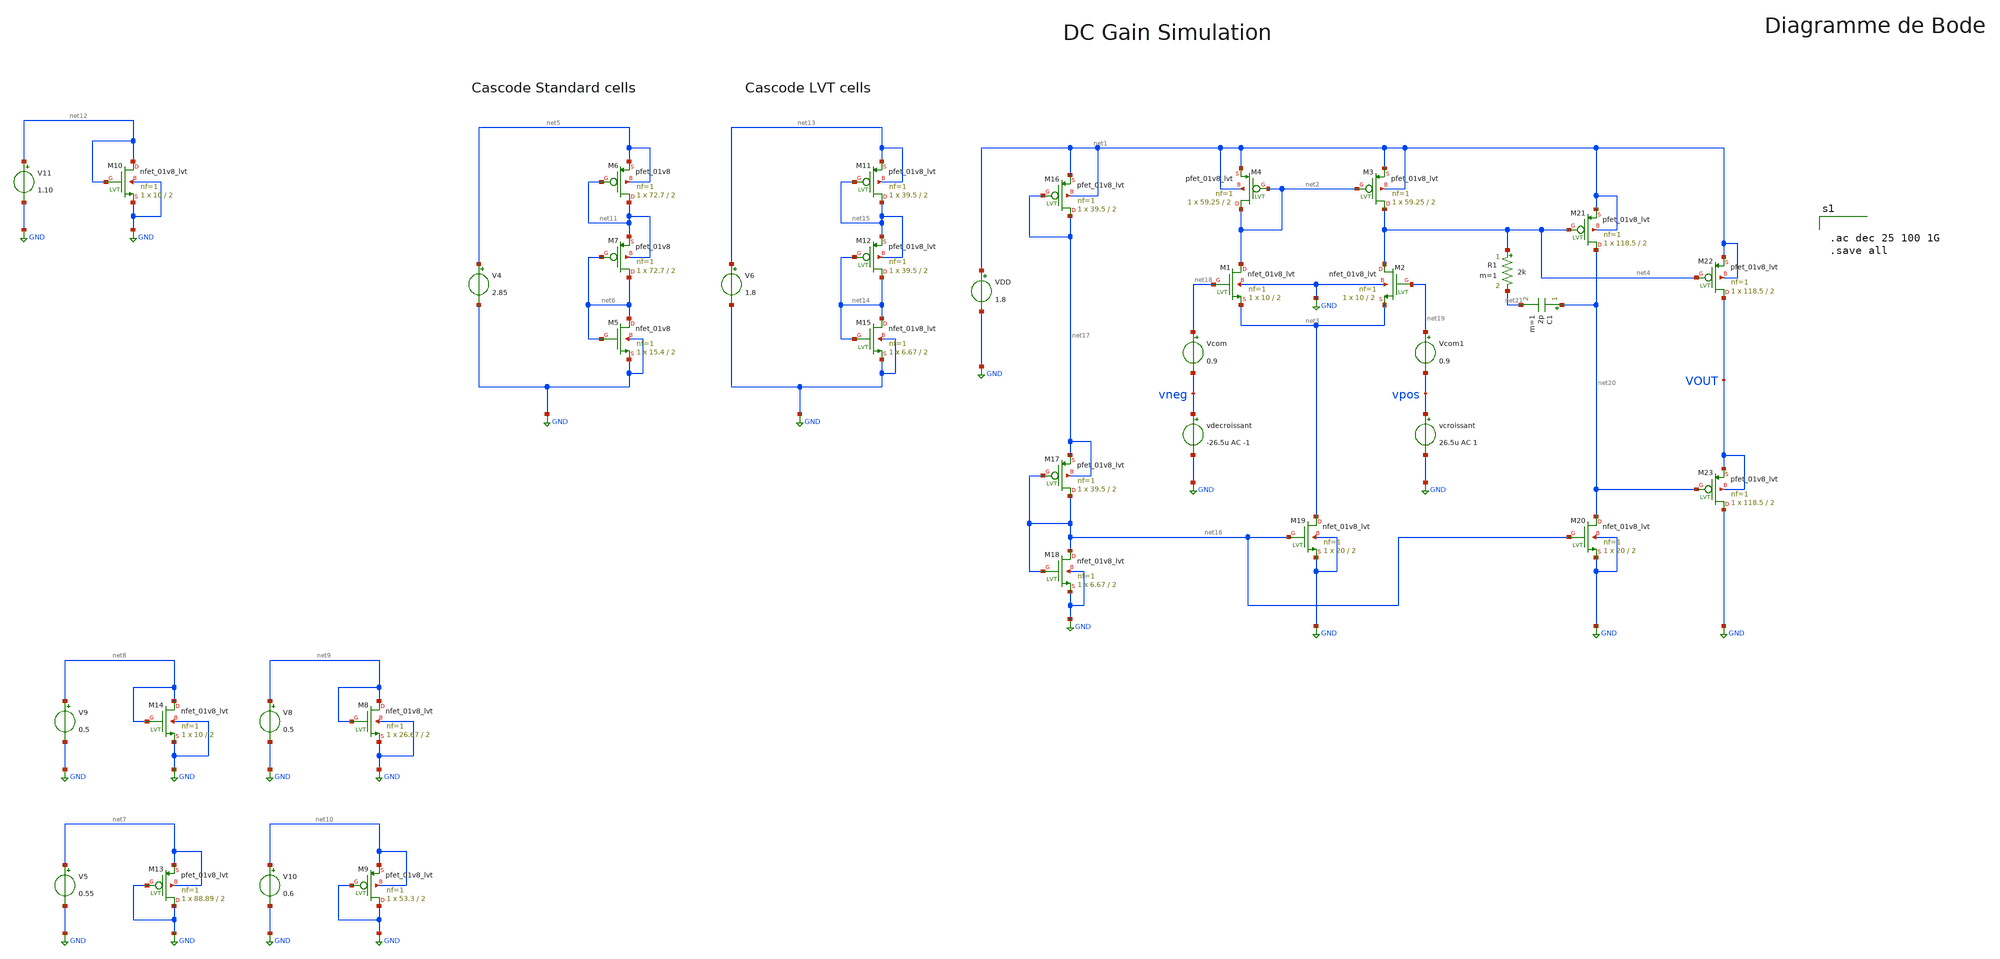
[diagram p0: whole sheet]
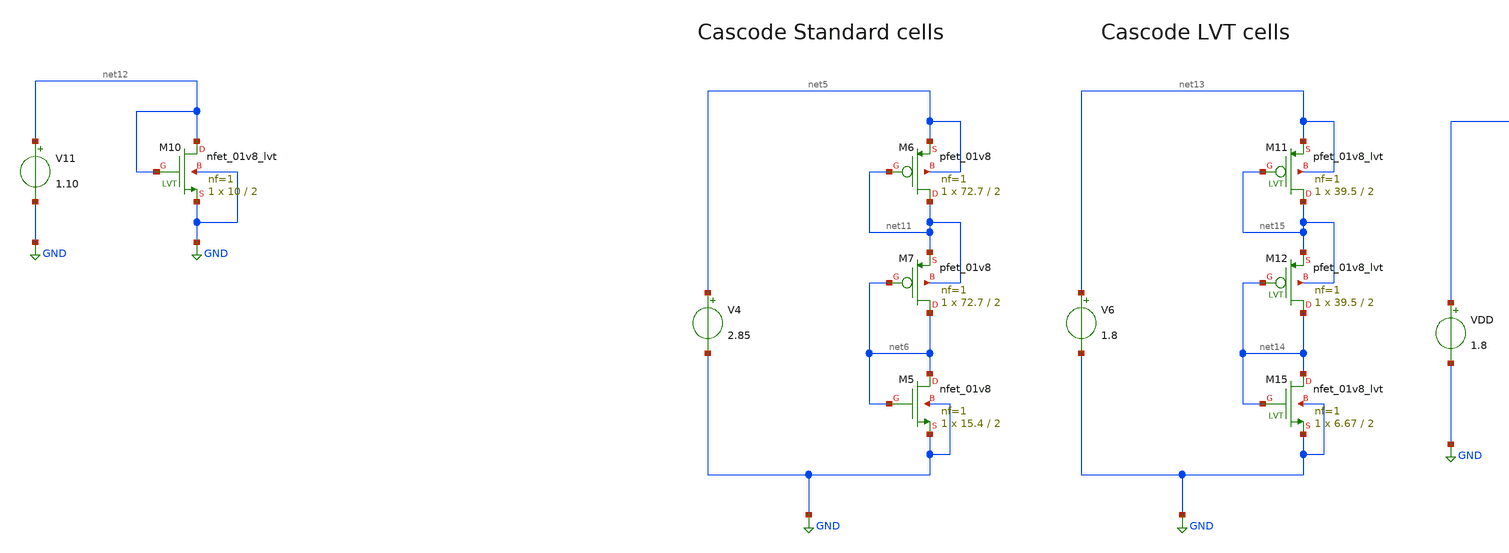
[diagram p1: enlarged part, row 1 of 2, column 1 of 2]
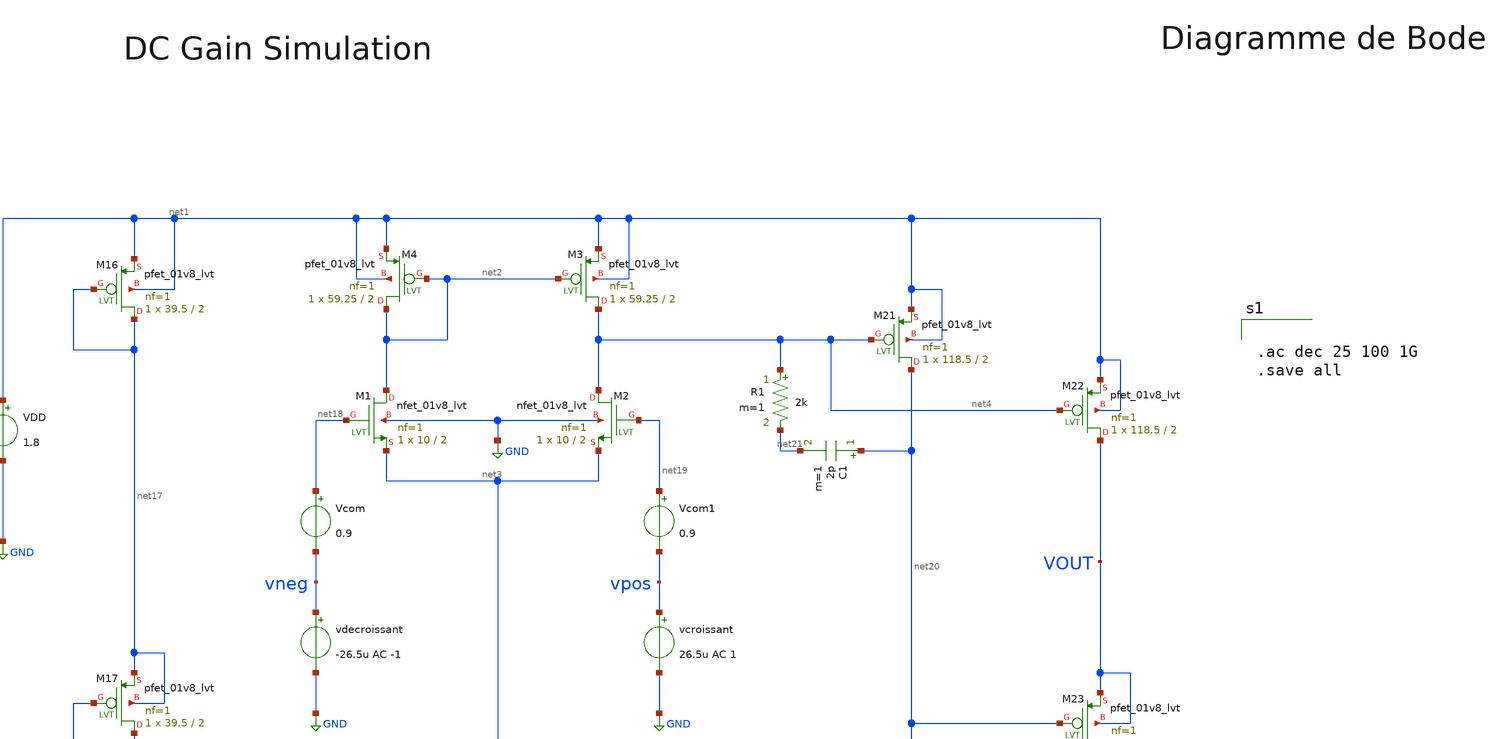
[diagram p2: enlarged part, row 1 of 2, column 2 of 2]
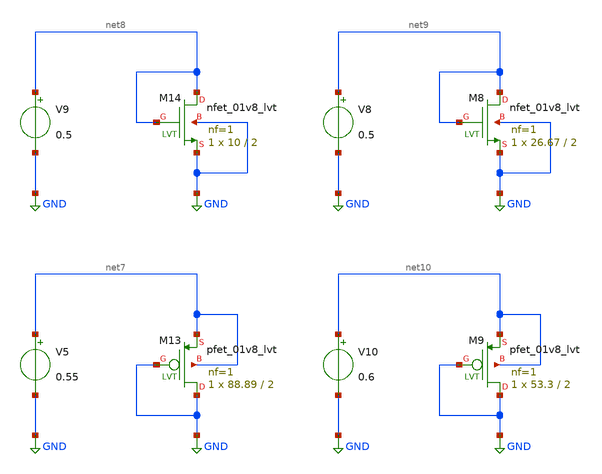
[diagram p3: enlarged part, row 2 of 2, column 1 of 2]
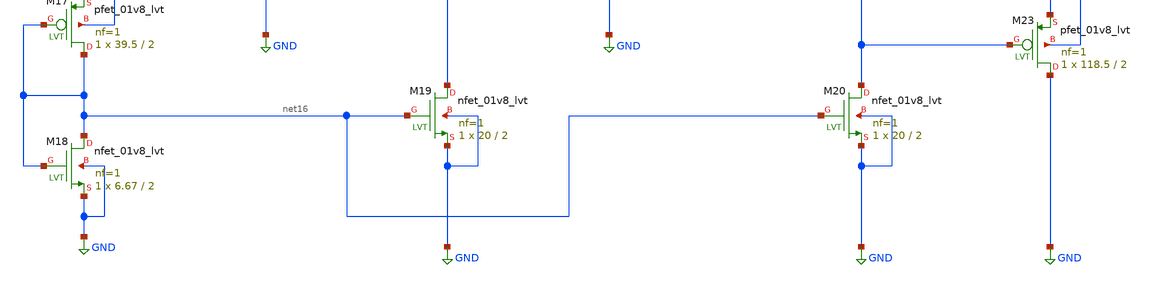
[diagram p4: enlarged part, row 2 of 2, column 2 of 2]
** sch_path: Paire_diff.sch
**.subckt Paire_diff
VDD net1 GND 1.8
V4 net5 GND 2.85
XM5 net6 net6 GND GND sky130_fd_pr__nfet_01v8 L=2 W=15.4 nf=1 ad='int((nf+1)/2) * W/nf * 0.29' as='int((nf+2)/2) * W/nf * 0.29'
+ pd='2*int((nf+1)/2) * (W/nf + 0.29)' ps='2*int((nf+2)/2) * (W/nf + 0.29)' nrd='0.29 / W' nrs='0.29 / W'
+ sa=0 sb=0 sd=0 mult=1 m=1
XM7 net6 net6 net11 net11 sky130_fd_pr__pfet_01v8 L=2 W=72.7 nf=1 ad='int((nf+1)/2) * W/nf * 0.29' as='int((nf+2)/2) * W/nf * 0.29'
+ pd='2*int((nf+1)/2) * (W/nf + 0.29)' ps='2*int((nf+2)/2) * (W/nf + 0.29)' nrd='0.29 / W' nrs='0.29 / W'
+ sa=0 sb=0 sd=0 mult=1 m=1
V5 net7 GND 0.55
V9 net8 GND 0.5
V8 net9 GND 0.5
V10 net10 GND 0.6
XM6 net11 net11 net5 net5 sky130_fd_pr__pfet_01v8 L=2 W=72.7 nf=1 ad='int((nf+1)/2) * W/nf * 0.29' as='int((nf+2)/2) * W/nf * 0.29'
+ pd='2*int((nf+1)/2) * (W/nf + 0.29)' ps='2*int((nf+2)/2) * (W/nf + 0.29)' nrd='0.29 / W' nrs='0.29 / W'
+ sa=0 sb=0 sd=0 mult=1 m=1
XM13 GND GND net7 net7 sky130_fd_pr__pfet_01v8_lvt L=2 W=88.89 nf=1 ad='int((nf+1)/2) * W/nf * 0.29'
+ as='int((nf+2)/2) * W/nf * 0.29' pd='2*int((nf+1)/2) * (W/nf + 0.29)' ps='2*int((nf+2)/2) * (W/nf + 0.29)'
+ nrd='0.29 / W' nrs='0.29 / W' sa=0 sb=0 sd=0 mult=1 m=1
XM14 net8 net8 GND GND sky130_fd_pr__nfet_01v8_lvt L=2 W=10 nf=1 ad='int((nf+1)/2) * W/nf * 0.29' as='int((nf+2)/2) * W/nf * 0.29'
+ pd='2*int((nf+1)/2) * (W/nf + 0.29)' ps='2*int((nf+2)/2) * (W/nf + 0.29)' nrd='0.29 / W' nrs='0.29 / W'
+ sa=0 sb=0 sd=0 mult=1 m=1
XM8 net9 net9 GND GND sky130_fd_pr__nfet_01v8_lvt L=2 W=26.67 nf=1 ad='int((nf+1)/2) * W/nf * 0.29' as='int((nf+2)/2) * W/nf * 0.29'
+ pd='2*int((nf+1)/2) * (W/nf + 0.29)' ps='2*int((nf+2)/2) * (W/nf + 0.29)' nrd='0.29 / W' nrs='0.29 / W'
+ sa=0 sb=0 sd=0 mult=1 m=1
XM9 GND GND net10 net10 sky130_fd_pr__pfet_01v8_lvt L=2 W=53.3 nf=1 ad='int((nf+1)/2) * W/nf * 0.29'
+ as='int((nf+2)/2) * W/nf * 0.29' pd='2*int((nf+1)/2) * (W/nf + 0.29)' ps='2*int((nf+2)/2) * (W/nf + 0.29)'
+ nrd='0.29 / W' nrs='0.29 / W' sa=0 sb=0 sd=0 mult=1 m=1
V11 net12 GND 1.10
XM10 net12 net12 GND GND sky130_fd_pr__nfet_01v8_lvt L=2 W=10 nf=1 ad='int((nf+1)/2) * W/nf * 0.29' as='int((nf+2)/2) * W/nf * 0.29'
+ pd='2*int((nf+1)/2) * (W/nf + 0.29)' ps='2*int((nf+2)/2) * (W/nf + 0.29)' nrd='0.29 / W' nrs='0.29 / W'
+ sa=0 sb=0 sd=0 mult=1 m=1
V6 net13 GND 1.8
XM11 net15 net15 net13 net13 sky130_fd_pr__pfet_01v8_lvt L=2 W=39.5 nf=1 ad='int((nf+1)/2) * W/nf * 0.29'
+ as='int((nf+2)/2) * W/nf * 0.29' pd='2*int((nf+1)/2) * (W/nf + 0.29)' ps='2*int((nf+2)/2) * (W/nf + 0.29)'
+ nrd='0.29 / W' nrs='0.29 / W' sa=0 sb=0 sd=0 mult=1 m=1
XM12 net14 net14 net15 net15 sky130_fd_pr__pfet_01v8_lvt L=2 W=39.5 nf=1 ad='int((nf+1)/2) * W/nf * 0.29'
+ as='int((nf+2)/2) * W/nf * 0.29' pd='2*int((nf+1)/2) * (W/nf + 0.29)' ps='2*int((nf+2)/2) * (W/nf + 0.29)'
+ nrd='0.29 / W' nrs='0.29 / W' sa=0 sb=0 sd=0 mult=1 m=1
XM15 net14 net14 GND GND sky130_fd_pr__nfet_01v8_lvt L=2 W=6.67 nf=1 ad='int((nf+1)/2) * W/nf * 0.29'
+ as='int((nf+2)/2) * W/nf * 0.29' pd='2*int((nf+1)/2) * (W/nf + 0.29)' ps='2*int((nf+2)/2) * (W/nf + 0.29)'
+ nrd='0.29 / W' nrs='0.29 / W' sa=0 sb=0 sd=0 mult=1 m=1
XM16 net17 net17 net1 net1 sky130_fd_pr__pfet_01v8_lvt L=2 W=39.5 nf=1 ad='int((nf+1)/2) * W/nf * 0.29'
+ as='int((nf+2)/2) * W/nf * 0.29' pd='2*int((nf+1)/2) * (W/nf + 0.29)' ps='2*int((nf+2)/2) * (W/nf + 0.29)'
+ nrd='0.29 / W' nrs='0.29 / W' sa=0 sb=0 sd=0 mult=1 m=1
XM17 net16 net16 net17 net17 sky130_fd_pr__pfet_01v8_lvt L=2 W=39.5 nf=1 ad='int((nf+1)/2) * W/nf * 0.29'
+ as='int((nf+2)/2) * W/nf * 0.29' pd='2*int((nf+1)/2) * (W/nf + 0.29)' ps='2*int((nf+2)/2) * (W/nf + 0.29)'
+ nrd='0.29 / W' nrs='0.29 / W' sa=0 sb=0 sd=0 mult=1 m=1
XM18 net16 net16 GND GND sky130_fd_pr__nfet_01v8_lvt L=2 W=6.67 nf=1 ad='int((nf+1)/2) * W/nf * 0.29'
+ as='int((nf+2)/2) * W/nf * 0.29' pd='2*int((nf+1)/2) * (W/nf + 0.29)' ps='2*int((nf+2)/2) * (W/nf + 0.29)'
+ nrd='0.29 / W' nrs='0.29 / W' sa=0 sb=0 sd=0 mult=1 m=1
XM19 net3 net16 GND GND sky130_fd_pr__nfet_01v8_lvt L=2 W=20 nf=1 ad='int((nf+1)/2) * W/nf * 0.29' as='int((nf+2)/2) * W/nf * 0.29'
+ pd='2*int((nf+1)/2) * (W/nf + 0.29)' ps='2*int((nf+2)/2) * (W/nf + 0.29)' nrd='0.29 / W' nrs='0.29 / W'
+ sa=0 sb=0 sd=0 mult=1 m=1
XM1 net2 net18 net3 GND sky130_fd_pr__nfet_01v8_lvt L=2 W=10 nf=1 ad='int((nf+1)/2) * W/nf * 0.29' as='int((nf+2)/2) * W/nf * 0.29'
+ pd='2*int((nf+1)/2) * (W/nf + 0.29)' ps='2*int((nf+2)/2) * (W/nf + 0.29)' nrd='0.29 / W' nrs='0.29 / W'
+ sa=0 sb=0 sd=0 mult=1 m=1
XM2 net4 net19 net3 GND sky130_fd_pr__nfet_01v8_lvt L=2 W=10 nf=1 ad='int((nf+1)/2) * W/nf * 0.29' as='int((nf+2)/2) * W/nf * 0.29'
+ pd='2*int((nf+1)/2) * (W/nf + 0.29)' ps='2*int((nf+2)/2) * (W/nf + 0.29)' nrd='0.29 / W' nrs='0.29 / W'
+ sa=0 sb=0 sd=0 mult=1 m=1
XM3 net4 net2 net1 net1 sky130_fd_pr__pfet_01v8_lvt L=2 W=59.25 nf=1 ad='int((nf+1)/2) * W/nf * 0.29'
+ as='int((nf+2)/2) * W/nf * 0.29' pd='2*int((nf+1)/2) * (W/nf + 0.29)' ps='2*int((nf+2)/2) * (W/nf + 0.29)'
+ nrd='0.29 / W' nrs='0.29 / W' sa=0 sb=0 sd=0 mult=1 m=1
XM4 net2 net2 net1 net1 sky130_fd_pr__pfet_01v8_lvt L=2 W=59.25 nf=1 ad='int((nf+1)/2) * W/nf * 0.29'
+ as='int((nf+2)/2) * W/nf * 0.29' pd='2*int((nf+1)/2) * (W/nf + 0.29)' ps='2*int((nf+2)/2) * (W/nf + 0.29)'
+ nrd='0.29 / W' nrs='0.29 / W' sa=0 sb=0 sd=0 mult=1 m=1
XM20 net20 net16 GND GND sky130_fd_pr__nfet_01v8_lvt L=2 W=20 nf=1 ad='int((nf+1)/2) * W/nf * 0.29' as='int((nf+2)/2) * W/nf * 0.29'
+ pd='2*int((nf+1)/2) * (W/nf + 0.29)' ps='2*int((nf+2)/2) * (W/nf + 0.29)' nrd='0.29 / W' nrs='0.29 / W'
+ sa=0 sb=0 sd=0 mult=1 m=1
XM21 net20 net4 net1 net1 sky130_fd_pr__pfet_01v8_lvt L=2 W=118.5 nf=1 ad='int((nf+1)/2) * W/nf * 0.29'
+ as='int((nf+2)/2) * W/nf * 0.29' pd='2*int((nf+1)/2) * (W/nf + 0.29)' ps='2*int((nf+2)/2) * (W/nf + 0.29)'
+ nrd='0.29 / W' nrs='0.29 / W' sa=0 sb=0 sd=0 mult=1 m=1
Vcom net18 vneg 0.9
XM22 VOUT net4 net1 net1 sky130_fd_pr__pfet_01v8_lvt L=2 W=118.5 nf=1 ad='int((nf+1)/2) * W/nf * 0.29'
+ as='int((nf+2)/2) * W/nf * 0.29' pd='2*int((nf+1)/2) * (W/nf + 0.29)' ps='2*int((nf+2)/2) * (W/nf + 0.29)'
+ nrd='0.29 / W' nrs='0.29 / W' sa=0 sb=0 sd=0 mult=1 m=1
XM23 GND net20 VOUT VOUT sky130_fd_pr__pfet_01v8_lvt L=2 W=118.5 nf=1 ad='int((nf+1)/2) * W/nf * 0.29'
+ as='int((nf+2)/2) * W/nf * 0.29' pd='2*int((nf+1)/2) * (W/nf + 0.29)' ps='2*int((nf+2)/2) * (W/nf + 0.29)'
+ nrd='0.29 / W' nrs='0.29 / W' sa=0 sb=0 sd=0 mult=1 m=1
Vcom1 net19 vpos 0.9
vcroissant vpos GND 26.5u AC 1
vdecroissant vneg GND -26.5u AC -1
C1 net20 net21 2p m=1
R1 net4 net21 2k m=1
**** begin user architecture code

** opencircuitdesign pdks install
.lib $::SKYWATER_MODELS/sky130.lib.spice tt



.ac dec 25 100 1G
.save all


**** end user architecture code
**.ends
.GLOBAL GND
.end
